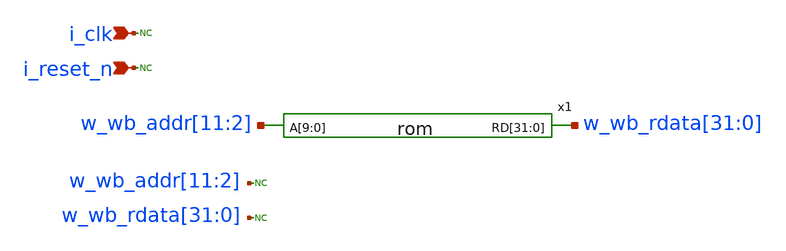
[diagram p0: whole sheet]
** sch_path: blocks/top/top.sch
**.subckt top i_clk i_reset_n
*.ipin i_clk
*.ipin i_reset_n
x1 w_wb_rdata[31] w_wb_rdata[30] w_wb_rdata[29] w_wb_rdata[28] w_wb_rdata[27] w_wb_rdata[26]
+ w_wb_rdata[25] w_wb_rdata[24] w_wb_rdata[23] w_wb_rdata[22] w_wb_rdata[21] w_wb_rdata[20] w_wb_rdata[19]
+ w_wb_rdata[18] w_wb_rdata[17] w_wb_rdata[16] w_wb_rdata[15] w_wb_rdata[14] w_wb_rdata[13] w_wb_rdata[12]
+ w_wb_rdata[11] w_wb_rdata[10] w_wb_rdata[9] w_wb_rdata[8] w_wb_rdata[7] w_wb_rdata[6] w_wb_rdata[5] w_wb_rdata[4]
+ w_wb_rdata[3] w_wb_rdata[2] w_wb_rdata[1] w_wb_rdata[0] w_wb_addr[11] w_wb_addr[10] w_wb_addr[9] w_wb_addr[8]
+ w_wb_addr[7] w_wb_addr[6] w_wb_addr[5] w_wb_addr[4] w_wb_addr[3] w_wb_addr[2] rom
* noconn i_clk
* noconn i_reset_n
* noconn w_wb_addr[11:2]
* noconn w_wb_rdata[31:0]
**** begin user architecture code

Xcore_wb VCC VSS i_clk i_reset_n w_wb_we w_wb_sel[0] w_wb_sel[1] w_wb_sel[2] w_wb_sel[3] w_wb_stb
+ w_wb_ack w_wb_cyc  w_wb_addr[0] w_wb_addr[1] w_wb_addr[2] w_wb_addr[3] w_wb_addr[4] w_wb_addr[5]
+ w_wb_addr[6] w_wb_addr[7] w_wb_addr[8] w_wb_addr[9] w_wb_addr[10] w_wb_addr[11] w_wb_addr[12] w_wb_addr[13]
+ w_wb_addr[14] w_wb_addr[15] w_wb_addr[16] w_wb_addr[17] w_wb_addr[18] w_wb_addr[19] w_wb_addr[20] w_wb_addr[21]
+ w_wb_addr[22] w_wb_addr[23] w_wb_addr[24] w_wb_addr[25] w_wb_addr[26] w_wb_addr[27] w_wb_addr[28] w_wb_addr[29]
+ w_wb_addr[30] w_wb_addr[31]  w_wb_wdata[0] w_wb_wdata[1] w_wb_wdata[2] w_wb_wdata[3] w_wb_wdata[4] w_wb_wdata[5]
+ w_wb_wdata[6] w_wb_wdata[7] w_wb_wdata[8] w_wb_wdata[9] w_wb_wdata[10] w_wb_wdata[11] w_wb_wdata[12]
+ w_wb_wdata[13] w_wb_wdata[14] w_wb_wdata[15] w_wb_wdata[16] w_wb_wdata[17] w_wb_wdata[18] w_wb_wdata[19]
+ w_wb_wdata[20] w_wb_wdata[21] w_wb_wdata[22] w_wb_wdata[23] w_wb_wdata[24] w_wb_wdata[25] w_wb_wdata[26]
+ w_wb_wdata[27] w_wb_wdata[28] w_wb_wdata[29] w_wb_wdata[30] w_wb_wdata[31]  w_wb_rdata[0] w_wb_rdata[1]
+ w_wb_rdata[2] w_wb_rdata[3] w_wb_rdata[4] w_wb_rdata[5] w_wb_rdata[6] w_wb_rdata[7] w_wb_rdata[8] w_wb_rdata[9]
+ w_wb_rdata[10] w_wb_rdata[11] w_wb_rdata[12] w_wb_rdata[13] w_wb_rdata[14] w_wb_rdata[15] w_wb_rdata[16]
+ w_wb_rdata[17] w_wb_rdata[18] w_wb_rdata[19] w_wb_rdata[20] w_wb_rdata[21] w_wb_rdata[22] w_wb_rdata[23]
+ w_wb_rdata[24] w_wb_rdata[25] w_wb_rdata[26] w_wb_rdata[27] w_wb_rdata[28] w_wb_rdata[29] w_wb_rdata[30]
+ w_wb_rdata[31]  rv_top_wb

Vw_wb_ack w_wb_ack 0 PWL 0n {VCC}

.include ./rv_top_wb.spice

**** end user architecture code
**.ends
.end
